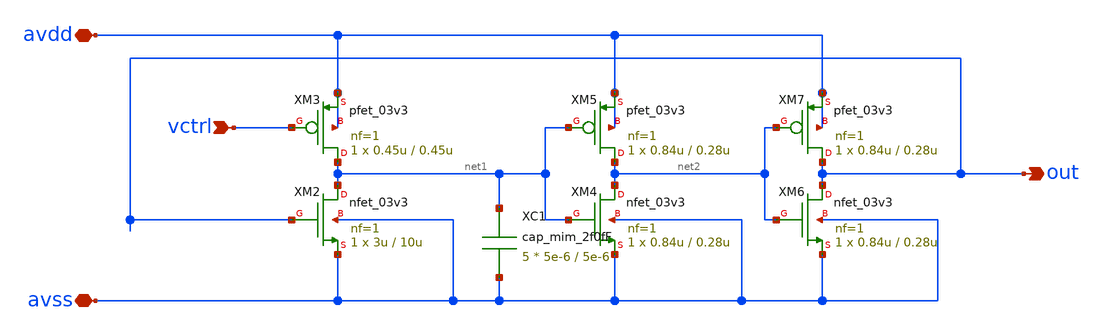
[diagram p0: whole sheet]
** sch_path: designs/libs/snn_analog/stdp/sch/stdp/vco.sch
**.subckt vco avdd avss vctrl out
*.iopin avdd
*.iopin avss
*.ipin vctrl
*.opin out
XM2 net1 out avss avss nfet_03v3 L=10u W=3u nf=1 ad='int((nf+1)/2) * W/nf * 0.18u' as='int((nf+2)/2) * W/nf * 0.18u'
+ pd='2*int((nf+1)/2) * (W/nf + 0.18u)' ps='2*int((nf+2)/2) * (W/nf + 0.18u)' nrd='0.18u / W' nrs='0.18u / W'
+ sa=0 sb=0 sd=0 m=1
XM3 net1 vctrl avdd avdd pfet_03v3 L=0.45u W=0.45u nf=1 ad='int((nf+1)/2) * W/nf * 0.18u' as='int((nf+2)/2) * W/nf * 0.18u'
+ pd='2*int((nf+1)/2) * (W/nf + 0.18u)' ps='2*int((nf+2)/2) * (W/nf + 0.18u)' nrd='0.18u / W' nrs='0.18u / W'
+ sa=0 sb=0 sd=0 m=1
XM4 net2 net1 avss avss nfet_03v3 L=0.28u W=0.84u nf=1 ad='int((nf+1)/2) * W/nf * 0.18u' as='int((nf+2)/2) * W/nf * 0.18u'
+ pd='2*int((nf+1)/2) * (W/nf + 0.18u)' ps='2*int((nf+2)/2) * (W/nf + 0.18u)' nrd='0.18u / W' nrs='0.18u / W'
+ sa=0 sb=0 sd=0 m=1
XM5 net2 net1 avdd avdd pfet_03v3 L=0.28u W=0.84u nf=1 ad='int((nf+1)/2) * W/nf * 0.18u' as='int((nf+2)/2) * W/nf * 0.18u'
+ pd='2*int((nf+1)/2) * (W/nf + 0.18u)' ps='2*int((nf+2)/2) * (W/nf + 0.18u)' nrd='0.18u / W' nrs='0.18u / W'
+ sa=0 sb=0 sd=0 m=1
XM6 out net2 avss avss nfet_03v3 L=0.28u W=0.84u nf=1 ad='int((nf+1)/2) * W/nf * 0.18u' as='int((nf+2)/2) * W/nf * 0.18u'
+ pd='2*int((nf+1)/2) * (W/nf + 0.18u)' ps='2*int((nf+2)/2) * (W/nf + 0.18u)' nrd='0.18u / W' nrs='0.18u / W'
+ sa=0 sb=0 sd=0 m=1
XM7 out net2 avdd avdd pfet_03v3 L=0.28u W=0.84u nf=1 ad='int((nf+1)/2) * W/nf * 0.18u' as='int((nf+2)/2) * W/nf * 0.18u'
+ pd='2*int((nf+1)/2) * (W/nf + 0.18u)' ps='2*int((nf+2)/2) * (W/nf + 0.18u)' nrd='0.18u / W' nrs='0.18u / W'
+ sa=0 sb=0 sd=0 m=1
XC1 net1 avss cap_mim_2f0fF c_width=5e-6 c_length=5e-6 m=5
**.ends
.end
